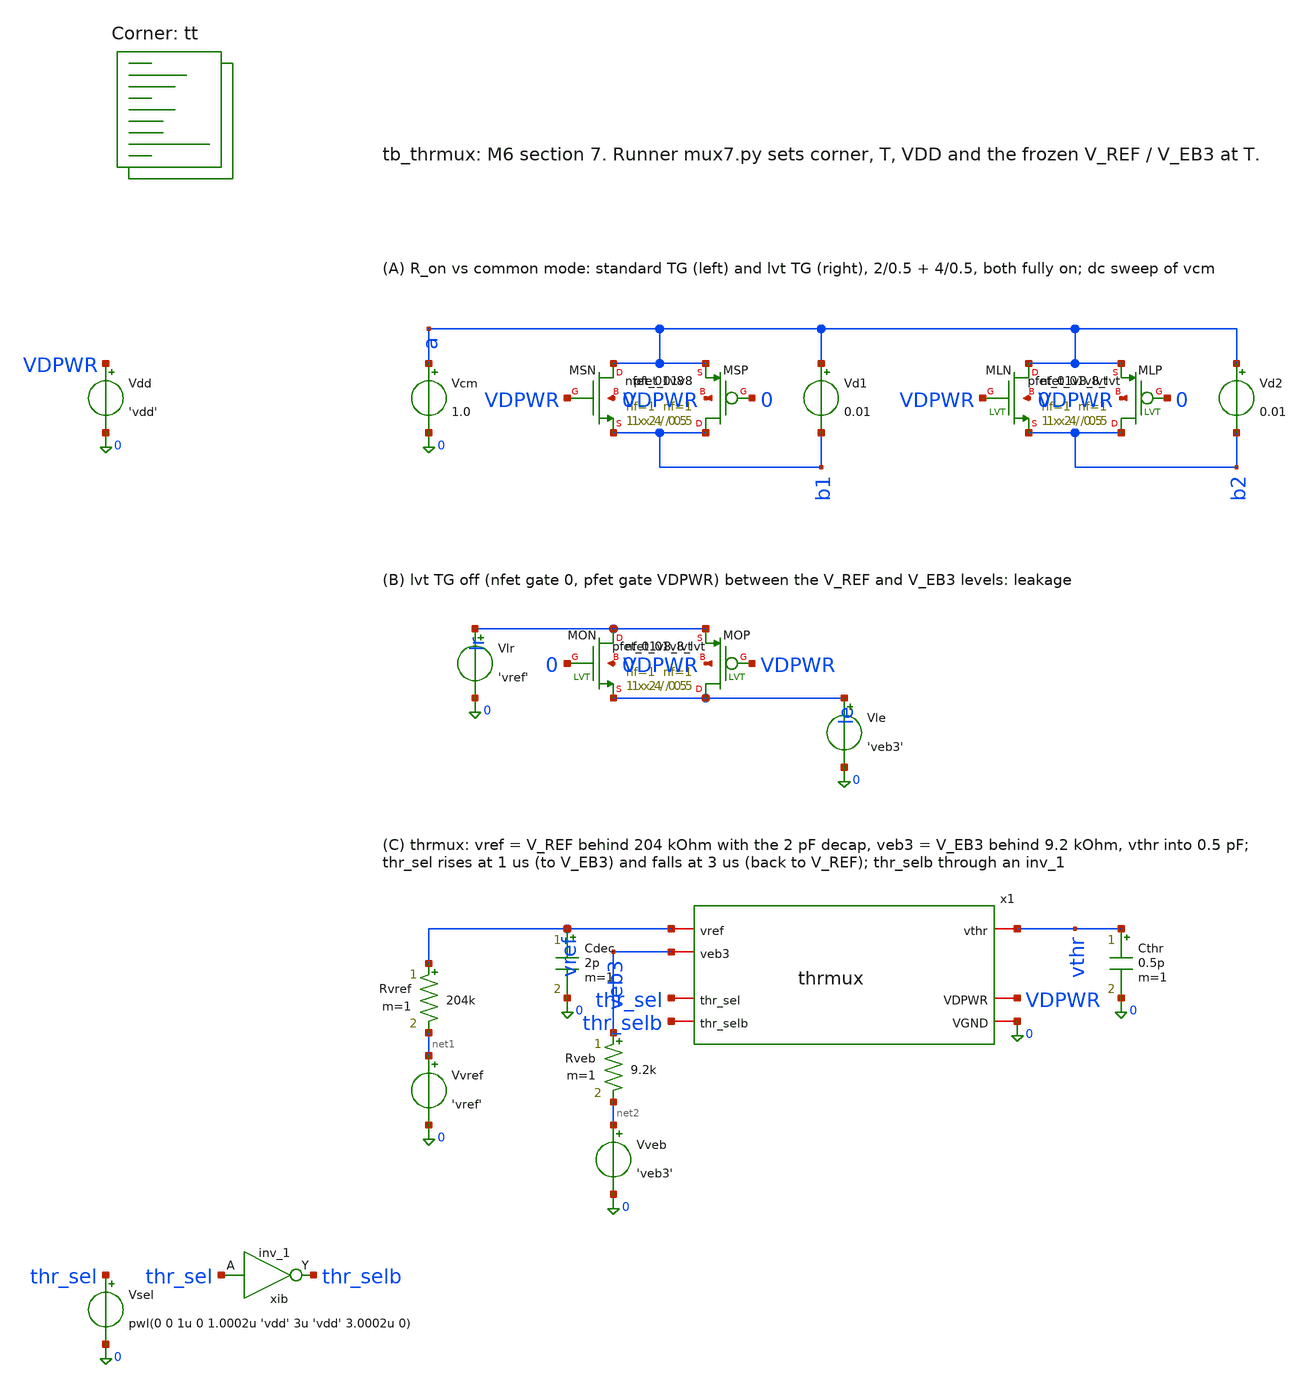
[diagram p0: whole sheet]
** sch_path: xschem/tb_thrmux.sch
**.subckt tb_thrmux
Vcm a 0 1.0
XMSN a VDPWR b1 0 sky130_fd_pr__nfet_01v8 L=0.5 W=2 nf=1 ad='int((1 + 1)/2) * 2 / 1 * 0.29' as='int((1 + 2)/2) * 2 / 1 * 0.29'
+ pd='2*int((1 + 1)/2) * (2 / 1 + 0.29)' ps='2*int((1 + 2)/2) * (2 / 1 + 0.29)' nrd='0.29 / 2 ' nrs='0.29 / 2 '
+ sa=0 sb=0 sd=0 mult=1 m=1
XMSP b1 0 a VDPWR sky130_fd_pr__pfet_01v8 L=0.5 W=4 nf=1 ad='int((1 + 1)/2) * 4 / 1 * 0.29' as='int((1 + 2)/2) * 4 / 1 * 0.29'
+ pd='2*int((1 + 1)/2) * (4 / 1 + 0.29)' ps='2*int((1 + 2)/2) * (4 / 1 + 0.29)' nrd='0.29 / 4 ' nrs='0.29 / 4 '
+ sa=0 sb=0 sd=0 mult=1 m=1
Vd1 a b1 0.01
XMLN a VDPWR b2 0 sky130_fd_pr__nfet_01v8_lvt L=0.5 W=2 nf=1 ad='int((1 + 1)/2) * 2 / 1 * 0.29' as='int((1 + 2)/2) * 2 / 1 * 0.29'
+ pd='2*int((1 + 1)/2) * (2 / 1 + 0.29)' ps='2*int((1 + 2)/2) * (2 / 1 + 0.29)' nrd='0.29 / 2 ' nrs='0.29 / 2 '
+ sa=0 sb=0 sd=0 mult=1 m=1
XMLP b2 0 a VDPWR sky130_fd_pr__pfet_01v8_lvt L=0.5 W=4 nf=1 ad='int((1 + 1)/2) * 4 / 1 * 0.29' as='int((1 + 2)/2) * 4 / 1 * 0.29'
+ pd='2*int((1 + 1)/2) * (4 / 1 + 0.29)' ps='2*int((1 + 2)/2) * (4 / 1 + 0.29)' nrd='0.29 / 4 ' nrs='0.29 / 4 '
+ sa=0 sb=0 sd=0 mult=1 m=1
Vd2 a b2 0.01
XMON lr 0 le 0 sky130_fd_pr__nfet_01v8_lvt L=0.5 W=2 nf=1 ad='int((1 + 1)/2) * 2 / 1 * 0.29' as='int((1 + 2)/2) * 2 / 1 * 0.29'
+ pd='2*int((1 + 1)/2) * (2 / 1 + 0.29)' ps='2*int((1 + 2)/2) * (2 / 1 + 0.29)' nrd='0.29 / 2 ' nrs='0.29 / 2 '
+ sa=0 sb=0 sd=0 mult=1 m=1
XMOP le VDPWR lr VDPWR sky130_fd_pr__pfet_01v8_lvt L=0.5 W=4 nf=1 ad='int((1 + 1)/2) * 4 / 1 * 0.29'
+ as='int((1 + 2)/2) * 4 / 1 * 0.29' pd='2*int((1 + 1)/2) * (4 / 1 + 0.29)' ps='2*int((1 + 2)/2) * (4 / 1 + 0.29)'
+ nrd='0.29 / 4 ' nrs='0.29 / 4 ' sa=0 sb=0 sd=0 mult=1 m=1
Vlr lr 0 'vref'
Vle le 0 'veb3'
x1 vref veb3 thr_sel thr_selb vthr VDPWR 0 thrmux
Vvref net1 0 'vref'
Rvref vref net1 204k m=1
Cdec vref 0 2p m=1
Vveb net2 0 'veb3'
Rveb veb3 net2 9.2k m=1
Cthr vthr 0 0.5p m=1
xib thr_sel 0 0 VDPWR VDPWR thr_selb sky130_fd_sc_hd__inv_1
Vsel thr_sel 0 pwl(0 0 1u 0 1.0002u 'vdd' 3u 'vdd' 3.0002u 0)
Vdd VDPWR 0 'vdd'
**** begin user architecture code
.lib $::SKYWATER_MODELS/sky130.lib.spice tt

.param vdd=1.8 vref=1.2432 veb3=0.7096
.include /foss/pdks/sky130A/libs.ref/sky130_fd_sc_hd/spice/sky130_fd_sc_hd.spice
.temp 25
.option method=gear
.control
dc vcm 0.5 1.3 0.005
let rs = 0.01/abs(i(vd1))
let rl = 0.01/abs(i(vd2))
meas dc rsmax max rs
meas dc rlmax max rl
meas dc rs096 find rs at=0.96
meas dc rl096 find rl at=0.96
echo RON rsmax=$&rsmax rlmax=$&rlmax rs096=$&rs096 rl096=$&rl096
wrdata ron_curve.txt rs rl
op
let ilr = abs(i(vlr))*1e9
let ile = abs(i(vle))*1e9
echo LEAK ilr_nA=$&ilr ile_nA=$&ile
tran 0.05n 8u 0 0.05n
meas tran a1 when v(x1.sref)=0.9 fall=1
meas tran a2 when v(x1.srefb)=0.9 rise=1
meas tran a3 when v(x1.seb)=0.9 rise=1
meas tran a4 when v(x1.sebb)=0.9 fall=1
meas tran b1 when v(x1.seb)=0.9 fall=1
meas tran b2 when v(x1.sebb)=0.9 rise=1
meas tran b3 when v(x1.sref)=0.9 rise=1
meas tran b4 when v(x1.srefb)=0.9 fall=1
meas tran s1 when v(vthr)=0.7097 fall=1 td=1u
meas tran s2 when v(vthr)=1.2431 rise=1 td=3u
meas tran vrmin min v(vref) from=3u to=4u
echo BBM a1=$&a1 a2=$&a2 a3=$&a3 a4=$&a4 b1=$&b1 b2=$&b2 b3=$&b3 b4=$&b4 s1=$&s1 s2=$&s2
+ vrmin=$&vrmin
.endc

**** end user architecture code
**.ends

* expanding   symbol:  thrmux.sym # of pins=7
** sym_path: xschem/thrmux.sym
** sch_path: xschem/thrmux.sch
.subckt thrmux vref veb3 thr_sel thr_selb vthr VDPWR VGND
*.ipin thr_sel
*.ipin thr_selb
*.ipin vref
*.ipin veb3
*.iopin vthr
*.iopin VDPWR
*.iopin VGND
xn1 thr_sel seb VGND VGND VDPWR VDPWR sref sky130_fd_sc_hd__nor2_1
xn2 sref thr_selb VGND VGND VDPWR VDPWR seb sky130_fd_sc_hd__nor2_1
xi1 sref VGND VGND VDPWR VDPWR srefb sky130_fd_sc_hd__inv_1
xi2 seb VGND VGND VDPWR VDPWR sebb sky130_fd_sc_hd__inv_1
XMTN1 vref sref vthr VGND sky130_fd_pr__nfet_01v8_lvt L=0.5 W=2 nf=1 ad='int((1 + 1)/2) * 2 / 1 * 0.29'
+ as='int((1 + 2)/2) * 2 / 1 * 0.29' pd='2*int((1 + 1)/2) * (2 / 1 + 0.29)' ps='2*int((1 + 2)/2) * (2 / 1 + 0.29)'
+ nrd='0.29 / 2 ' nrs='0.29 / 2 ' sa=0 sb=0 sd=0 mult=1 m=1
XMTP1 vthr srefb vref VDPWR sky130_fd_pr__pfet_01v8_lvt L=0.5 W=4 nf=1 ad='int((1 + 1)/2) * 4 / 1 * 0.29'
+ as='int((1 + 2)/2) * 4 / 1 * 0.29' pd='2*int((1 + 1)/2) * (4 / 1 + 0.29)' ps='2*int((1 + 2)/2) * (4 / 1 + 0.29)'
+ nrd='0.29 / 4 ' nrs='0.29 / 4 ' sa=0 sb=0 sd=0 mult=1 m=1
XMTN2 vthr seb veb3 VGND sky130_fd_pr__nfet_01v8_lvt L=0.5 W=2 nf=1 ad='int((1 + 1)/2) * 2 / 1 * 0.29'
+ as='int((1 + 2)/2) * 2 / 1 * 0.29' pd='2*int((1 + 1)/2) * (2 / 1 + 0.29)' ps='2*int((1 + 2)/2) * (2 / 1 + 0.29)'
+ nrd='0.29 / 2 ' nrs='0.29 / 2 ' sa=0 sb=0 sd=0 mult=1 m=1
XMTP2 veb3 sebb vthr VDPWR sky130_fd_pr__pfet_01v8_lvt L=0.5 W=4 nf=1 ad='int((1 + 1)/2) * 4 / 1 * 0.29'
+ as='int((1 + 2)/2) * 4 / 1 * 0.29' pd='2*int((1 + 1)/2) * (4 / 1 + 0.29)' ps='2*int((1 + 2)/2) * (4 / 1 + 0.29)'
+ nrd='0.29 / 4 ' nrs='0.29 / 4 ' sa=0 sb=0 sd=0 mult=1 m=1
.ends

.end
